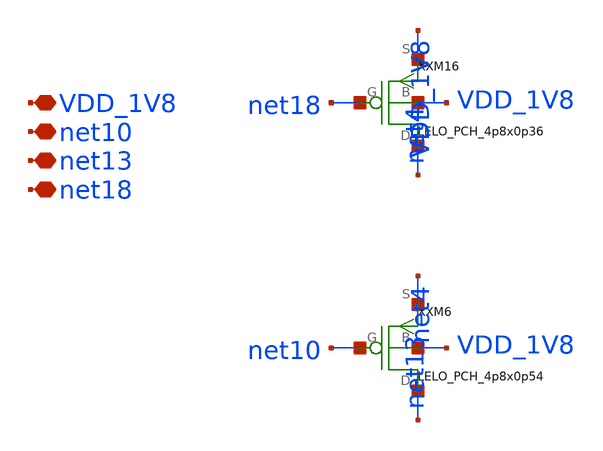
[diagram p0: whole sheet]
** sch_path: design/LELO_VCO_SKY130A/LELO_VCO_PA1.sch
**.subckt LELO_VCO_PA1 VDD_1V8 net10 net13 net18
*.iopin VDD_1V8
*.iopin net10
*.iopin net13
*.iopin net18
XXXM16 net4 net18 VDD_1V8 VDD_1V8 LELO_PCH_4p8x0p36
XXM6 net13 net10 net4 VDD_1V8 LELO_PCH_4p8x0p54
**.ends

* expanding   symbol:  LELO_VCO_SKY130A/LELO_PCH_4p8x0p36.sym # of pins=4
** sym_path: design/LELO_VCO_SKY130A/LELO_PCH_4p8x0p36.sym
** sch_path: design/LELO_VCO_SKY130A/LELO_PCH_4p8x0p36.sch
.subckt LELO_PCH_4p8x0p36 D G S B
*.iopin D
*.iopin G
*.iopin S
*.iopin B
XM1 D G S B sky130_fd_pr__pfet_01v8 L=0.36 W=4.8 nf=1 ad='int((nf+1)/2) * W/nf * 0.29' as='int((nf+2)/2) * W/nf * 0.29'
+ pd='2*int((nf+1)/2) * (W/nf + 0.29)' ps='2*int((nf+2)/2) * (W/nf + 0.29)' nrd='0.29 / W' nrs='0.29 / W'
+ sa=0 sb=0 sd=0 mult=1 m=1
.ends


* expanding   symbol:  LELO_VCO_SKY130A/LELO_PCH_4p8x0p54.sym # of pins=4
** sym_path: design/LELO_VCO_SKY130A/LELO_PCH_4p8x0p54.sym
** sch_path: design/LELO_VCO_SKY130A/LELO_PCH_4p8x0p54.sch
.subckt LELO_PCH_4p8x0p54 D G S B
*.iopin D
*.iopin G
*.iopin S
*.iopin B
XM1 D G S B sky130_fd_pr__pfet_01v8 L=0.54 W=4.8 nf=1 ad='int((nf+1)/2) * W/nf * 0.29' as='int((nf+2)/2) * W/nf * 0.29'
+ pd='2*int((nf+1)/2) * (W/nf + 0.29)' ps='2*int((nf+2)/2) * (W/nf + 0.29)' nrd='0.29 / W' nrs='0.29 / W'
+ sa=0 sb=0 sd=0 mult=1 m=1
.ends

.end
